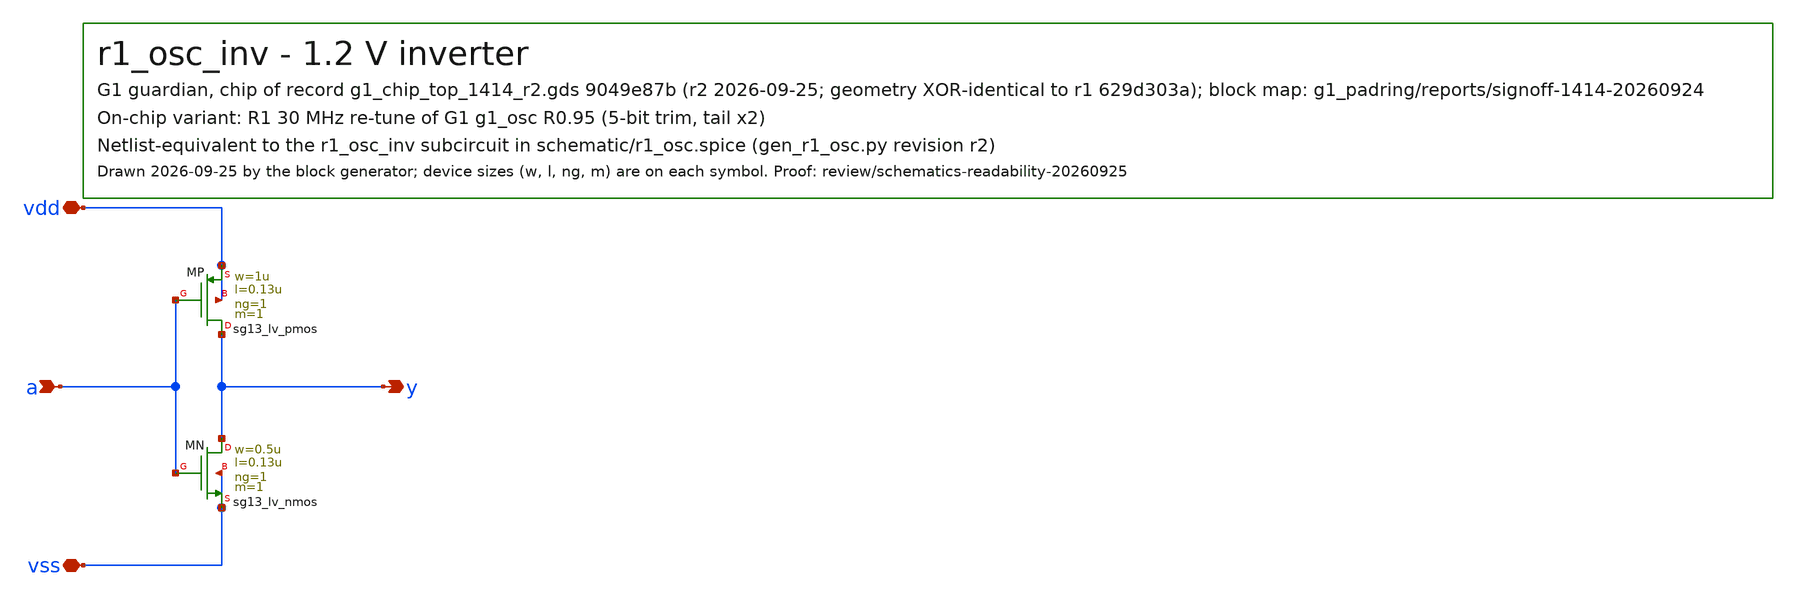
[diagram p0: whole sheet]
** sch_path: designs/r1-joint/blocks/r1_osc/schematic/r1_osc_inv.sch
**.subckt r1_osc_inv a y vdd vss
*.ipin a
*.opin y
*.iopin vdd
*.iopin vss
XMP y a vdd vdd sg13_lv_pmos w=1u l=0.13u ng=1 m=1 mm_ok=1
XMN y a vss vss sg13_lv_nmos w=0.5u l=0.13u ng=1 m=1 mm_ok=1
**.ends
.end
